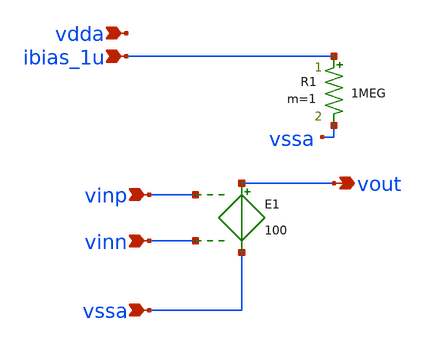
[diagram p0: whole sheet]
** sch_path: Running_closed_loop_stability_analysis_in_ngspice_through_xschem/OTA_ideal_order0_elmod.sch
**.subckt OTA_ideal_order0_elmod vssa vinp vout ibias_1u vinn vdda
*.ipin vssa
*.ipin vinp
*.opin vout
*.ipin ibias_1u
*.ipin vinn
*.ipin vdda
E1 vout vssa vinp vinn 100
R1 ibias_1u vssa 1MEG m=1
**.ends
.end
